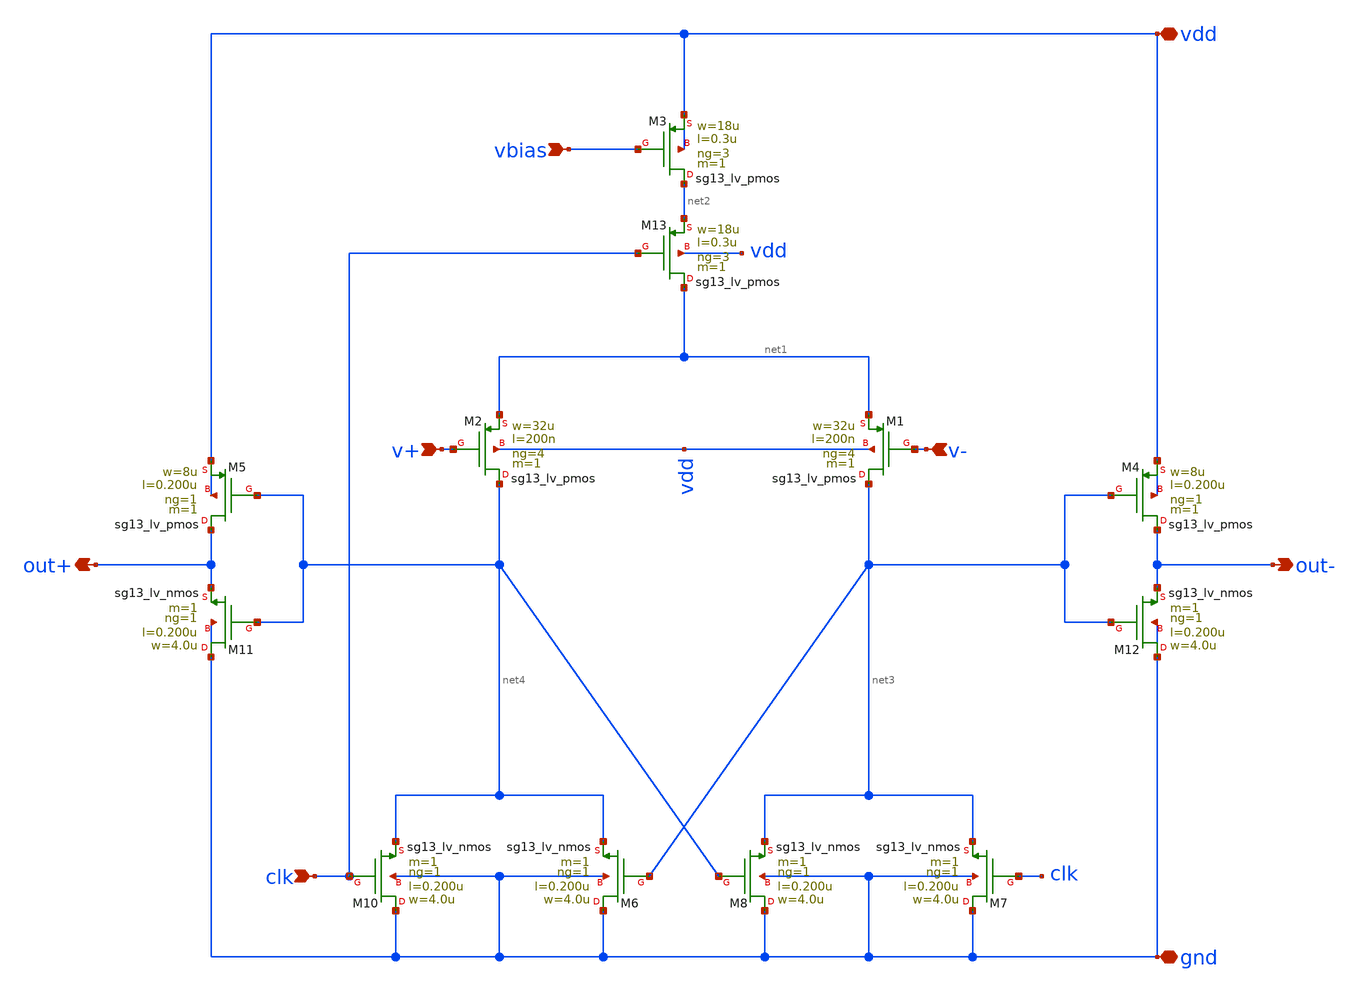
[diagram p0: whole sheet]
** sch_path: modules/module_3_8_bit_SAR_ADC/part_5_layout/components/comparator/schematic/dynamic_comparator.sch
**.subckt dynamic_comparator vdd gnd v+ v- vbias clk out- out+
*.iopin vdd
*.iopin gnd
*.ipin v+
*.ipin v-
*.ipin vbias
*.ipin clk
*.opin out-
*.opin out+
XM13 net1 clk net2 vdd sg13_lv_pmos w=18u l=0.3u ng=3 m=1 mm_ok=1
XM3 net2 vbias vdd vdd sg13_lv_pmos w=18u l=0.3u ng=3 m=1 mm_ok=1
XM2 net4 v+ net1 vdd sg13_lv_pmos w=32u l=200n ng=4 m=1 mm_ok=1
XM1 net3 v- net1 vdd sg13_lv_pmos w=32u l=200n ng=4 m=1 mm_ok=1
XM4 out- net3 vdd vdd sg13_lv_pmos w=8u l=0.200u ng=1 m=1 mm_ok=1
XM5 out+ net4 vdd vdd sg13_lv_pmos w=8u l=0.200u ng=1 m=1 mm_ok=1
XM11 gnd net4 out+ gnd sg13_lv_nmos w=4.0u l=0.200u ng=1 m=1 mm_ok=1
XM12 gnd net3 out- gnd sg13_lv_nmos w=4.0u l=0.200u ng=1 m=1 mm_ok=1
XM6 gnd net3 net4 gnd sg13_lv_nmos w=4.0u l=0.200u ng=1 m=1 mm_ok=1
XM10 gnd clk net4 gnd sg13_lv_nmos w=4.0u l=0.200u ng=1 m=1 mm_ok=1
XM7 gnd clk net3 gnd sg13_lv_nmos w=4.0u l=0.200u ng=1 m=1 mm_ok=1
XM8 gnd net4 net3 gnd sg13_lv_nmos w=4.0u l=0.200u ng=1 m=1 mm_ok=1
**.ends
.end
